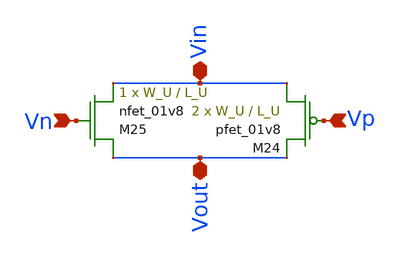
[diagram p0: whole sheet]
** sch_path: schematics/switch.sch
**.subckt switch Vin Vout Vp Vn
*.iopin Vin
*.iopin Vout
*.ipin Vp
*.ipin Vn
XM24 Vin Vp Vout VDD sky130_fd_pr__pfet_01v8 L=L_U W=W_U nf=1 ad='int((nf+1)/2) * W/nf * 0.29' as='int((nf+2)/2) * W/nf * 0.29'
+ pd='2*int((nf+1)/2) * (W/nf + 0.29)' ps='2*int((nf+2)/2) * (W/nf + 0.29)' nrd='0.29 / W' nrs='0.29 / W'
+ sa=0 sb=0 sd=0 mult=2 m=2
XM25 Vout Vn Vin GND sky130_fd_pr__nfet_01v8 L=L_U W=W_U nf=1 ad='int((nf+1)/2) * W/nf * 0.29' as='int((nf+2)/2) * W/nf * 0.29'
+ pd='2*int((nf+1)/2) * (W/nf + 0.29)' ps='2*int((nf+2)/2) * (W/nf + 0.29)' nrd='0.29 / W' nrs='0.29 / W'
+ sa=0 sb=0 sd=0 mult=1 m=1
**.ends
.end
